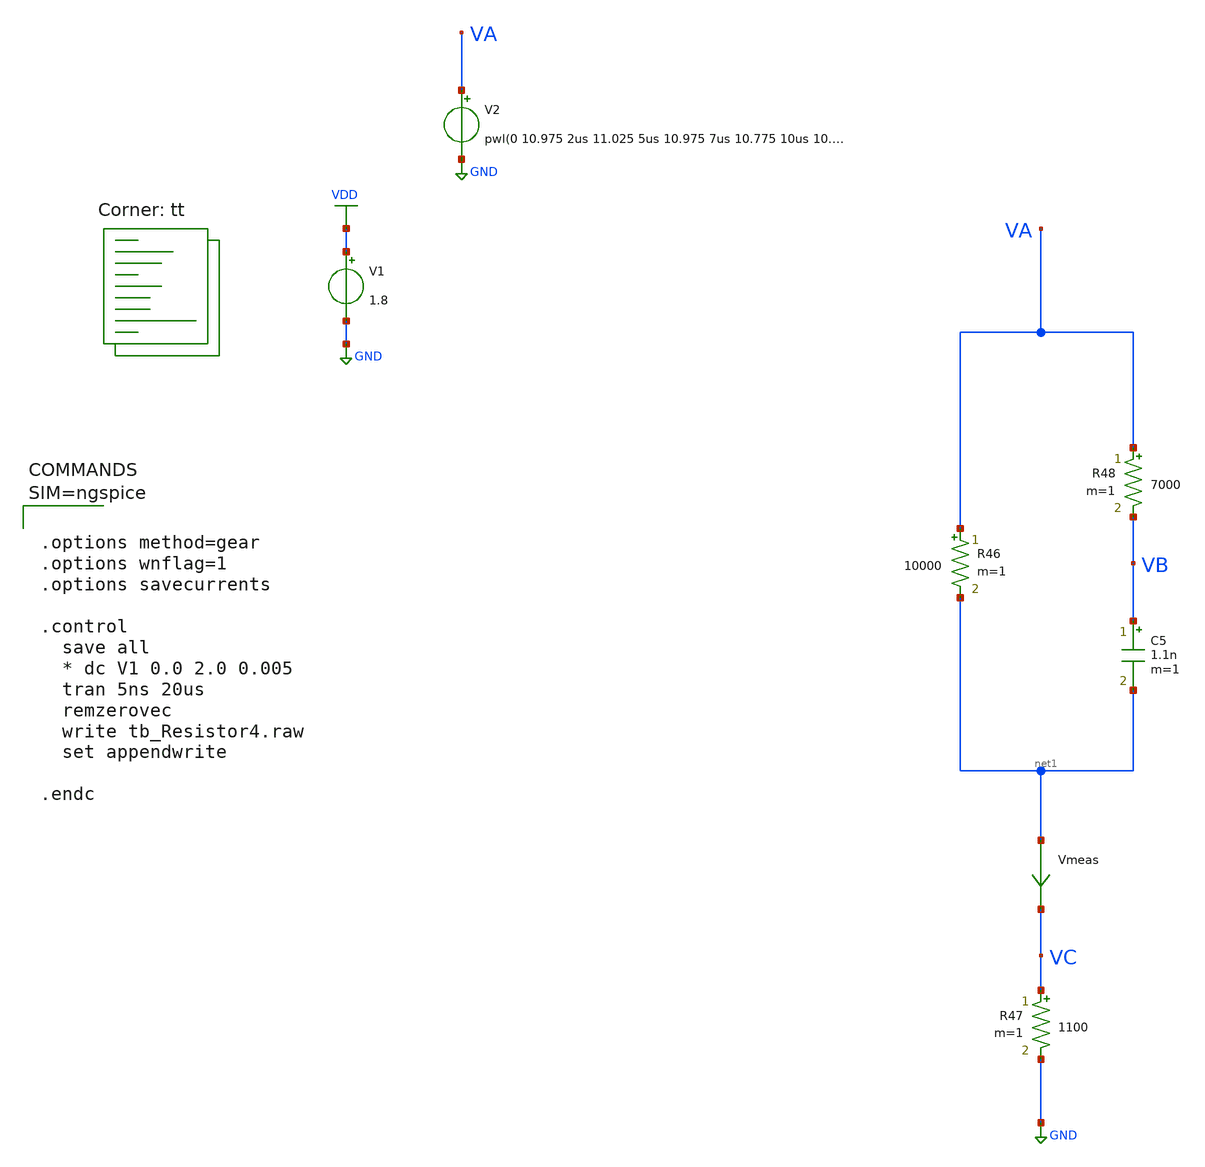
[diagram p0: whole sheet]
** sch_path: projects/ASU/EEE572/schematic/tb_Resistor4.sch
**.subckt tb_Resistor4
V1 VDD GND 1.8
V2 VA GND pwl(0 10.975 2us 11.025 5us 10.975 7us 10.775 10us 10.725 12us 10.525 15us 10.475 17us
+ 10.275 20us 10.225)
R46 VA net1 10000 m=1
R47 VC GND 1100 m=1
R48 VA VB 7000 m=1
C5 VB net1 1.1n m=1
Vmeas net1 VC 0
.save i(vmeas)
**** begin user architecture code
.lib $::SKYWATER_MODELS/sky130.lib.spice tt



.options method=gear
.options wnflag=1
.options savecurrents

.control
  save all
  * dc V1 0.0 2.0 0.005
  tran 5ns 20us
  remzerovec
  write tb_Resistor4.raw
  set appendwrite

.endc





**** end user architecture code
**.ends
.GLOBAL GND
.GLOBAL VDD
.end
